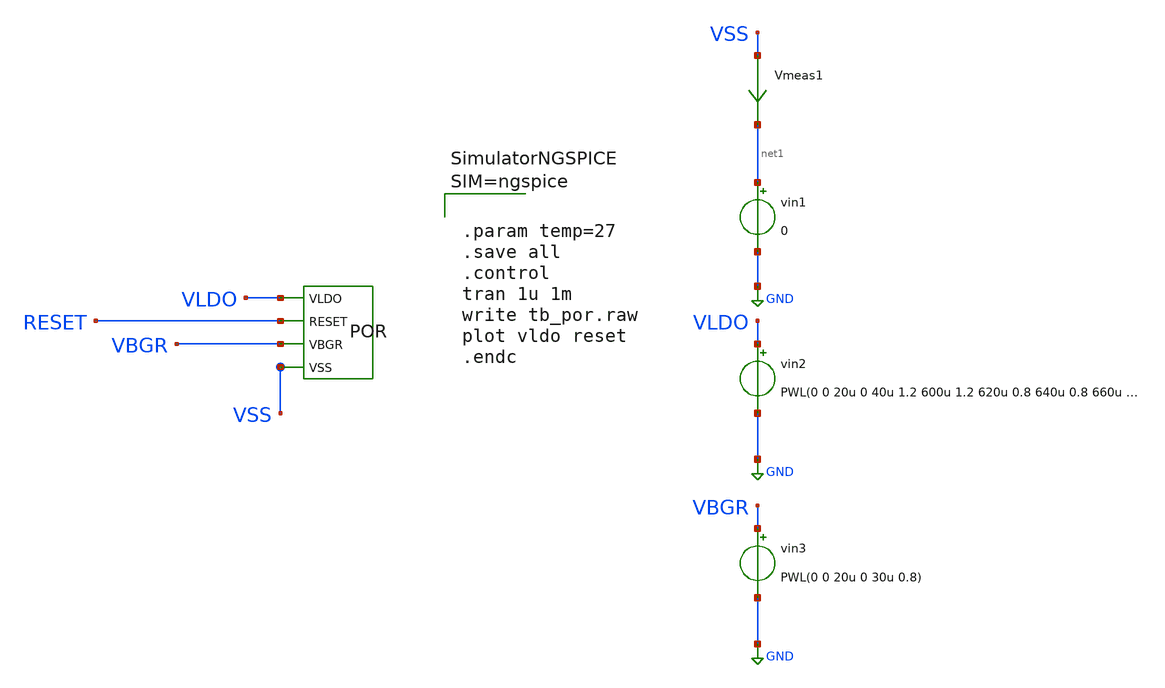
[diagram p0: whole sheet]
** sch_path: dependencies/POR/POR-main/testbenches/tran/xschem/por_post_layout_sim_tran.sch
**.subckt por_post_layout_sim_tran
X1 VLDO RESET VBGR VSS POR
vin1 net1 GND 0
Vmeas1 VSS net1 0
.save i(vmeas1)
vin2 VLDO GND PWL(0 0 20u 0 40u 1.2 600u 1.2 620u 0.8 640u 0.8 660u 1.2 760u 1.2 780u 0)
vin3 VBGR GND PWL(0 0 20u 0 30u 0.8)
**** begin user architecture code



.include /foss/designs/simulations/POR/output/POR__POR/magic_RC/POR.pex.spice
.lib cornerMOSlv.lib mos_tt
.lib cornerMOShv.lib mos_tt
.lib cornerHBT.lib hbt_typ
.lib cornerRES.lib res_typ
.lib cornerDIO.lib dio_tt
.lib cornerCAP.lib cap_typ






.param temp=27
.save all
.control
tran 1u 1m
write tb_por.raw
plot vldo reset
.endc



**** end user architecture code
**.ends
.GLOBAL GND
.end
